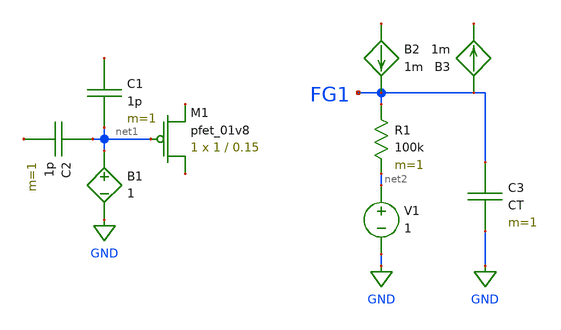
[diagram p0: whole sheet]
** sch_path: schematic/floating_gate.sch
**.subckt floating_gate
XM1 net3 net1 net4 VDD sky130_fd_pr__pfet_01v8 L=0.15 W=1 nf=1 ad='int((nf+1)/2) * W/nf * 0.29' as='int((nf+2)/2) * W/nf * 0.29'
+ pd='2*int((nf+1)/2) * (W/nf + 0.29)' ps='2*int((nf+2)/2) * (W/nf + 0.29)' nrd='0.29 / W' nrs='0.29 / W'
+ sa=0 sb=0 sd=0 mult=1 m=1
C1 net5 net1 1p m=1
C2 net1 net6 1p m=1
B1 net1 GND V=1
R1 FG1 net2 100k m=1
V1 net2 GND 1
C3 FG1 GND CT m=1
B2 net7 FG1 I=1m
B3 FG1 net8 I=1m
**.ends
.GLOBAL GND
.end
